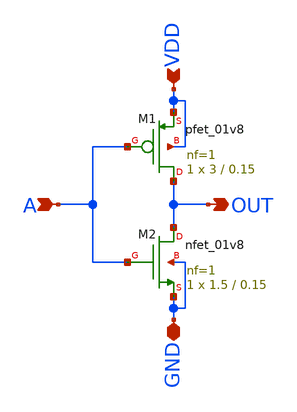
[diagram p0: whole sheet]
** sch_path: skywater_stuff/CMOS_INV.sch
**.subckt CMOS_INV GND A VDD OUT
*.iopin GND
*.ipin A
*.ipin VDD
*.opin OUT
XM1 OUT A VDD VDD sky130_fd_pr__pfet_01v8 L=0.15 W=3 nf=1 ad='int((nf+1)/2) * W/nf * 0.29' as='int((nf+2)/2) * W/nf * 0.29'
+ pd='2*int((nf+1)/2) * (W/nf + 0.29)' ps='2*int((nf+2)/2) * (W/nf + 0.29)' nrd='0.29 / W' nrs='0.29 / W'
+ sa=0 sb=0 sd=0 mult=1 m=1
XM2 OUT A GND GND sky130_fd_pr__nfet_01v8 L=0.15 W=1.5 nf=1 ad='int((nf+1)/2) * W/nf * 0.29' as='int((nf+2)/2) * W/nf * 0.29'
+ pd='2*int((nf+1)/2) * (W/nf + 0.29)' ps='2*int((nf+2)/2) * (W/nf + 0.29)' nrd='0.29 / W' nrs='0.29 / W'
+ sa=0 sb=0 sd=0 mult=1 m=1
**.ends
.end
